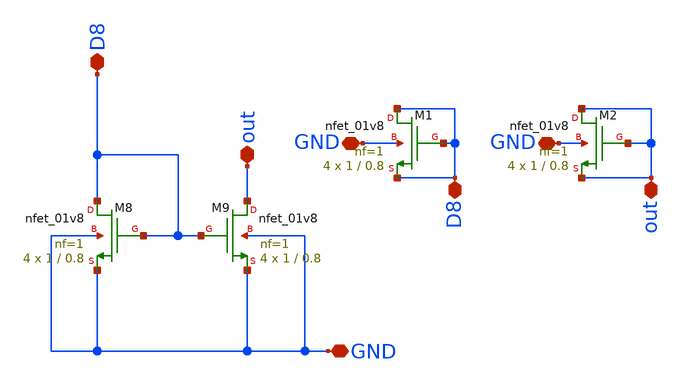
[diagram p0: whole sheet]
** sch_path: mag/lnmos.sch
**.subckt lnmos GND D8 out GND GND D8 out
*.iopin GND
*.iopin D8
*.iopin out
*.iopin GND
*.iopin GND
*.iopin D8
*.iopin out
XM8 D8 D8 GND GND sky130_fd_pr__nfet_01v8 L=0.8 W=1 nf=1 ad='int((nf+1)/2) * W/nf * 0.29' as='int((nf+2)/2) * W/nf * 0.29'
+ pd='2*int((nf+1)/2) * (W/nf + 0.29)' ps='2*int((nf+2)/2) * (W/nf + 0.29)' nrd='0.29 / W' nrs='0.29 / W'
+ sa=0 sb=0 sd=0 mult=4 m=4
XM9 out D8 GND GND sky130_fd_pr__nfet_01v8 L=0.8 W=1 nf=1 ad='int((nf+1)/2) * W/nf * 0.29' as='int((nf+2)/2) * W/nf * 0.29'
+ pd='2*int((nf+1)/2) * (W/nf + 0.29)' ps='2*int((nf+2)/2) * (W/nf + 0.29)' nrd='0.29 / W' nrs='0.29 / W'
+ sa=0 sb=0 sd=0 mult=4 m=4
XM1 D8 D8 D8 GND sky130_fd_pr__nfet_01v8 L=0.8 W=1 nf=1 ad='int((nf+1)/2) * W/nf * 0.29' as='int((nf+2)/2) * W/nf * 0.29'
+ pd='2*int((nf+1)/2) * (W/nf + 0.29)' ps='2*int((nf+2)/2) * (W/nf + 0.29)' nrd='0.29 / W' nrs='0.29 / W'
+ sa=0 sb=0 sd=0 mult=4 m=4
XM2 out out out GND sky130_fd_pr__nfet_01v8 L=0.8 W=1 nf=1 ad='int((nf+1)/2) * W/nf * 0.29' as='int((nf+2)/2) * W/nf * 0.29'
+ pd='2*int((nf+1)/2) * (W/nf + 0.29)' ps='2*int((nf+2)/2) * (W/nf + 0.29)' nrd='0.29 / W' nrs='0.29 / W'
+ sa=0 sb=0 sd=0 mult=4 m=4
**.ends
.end
